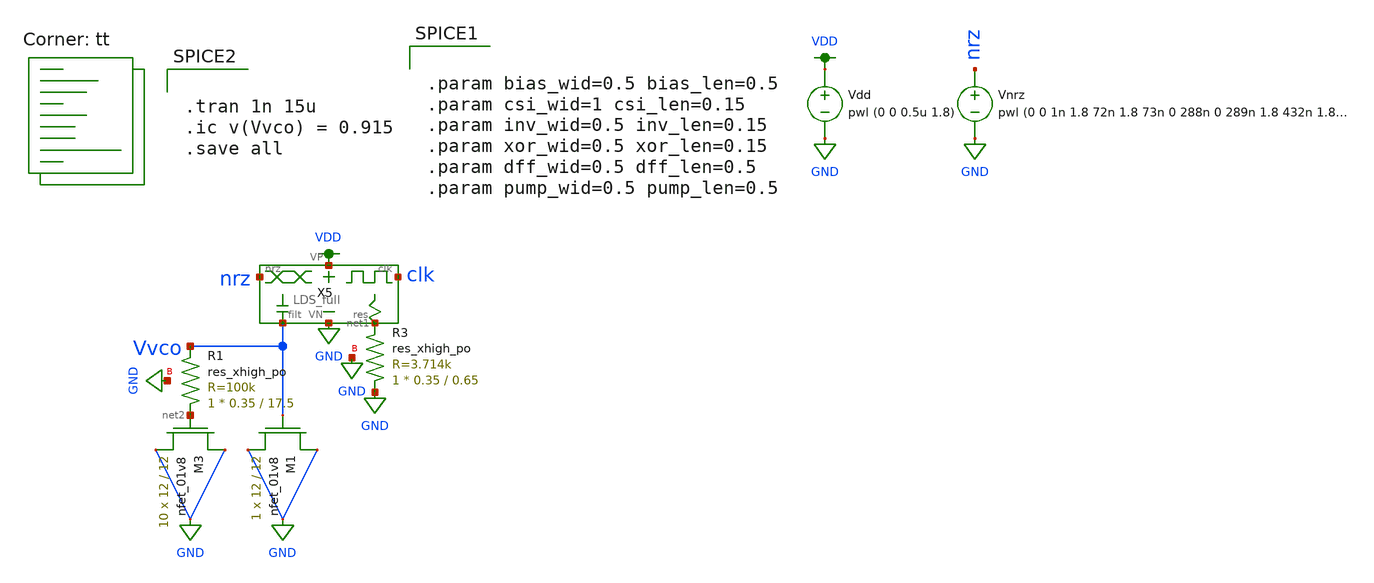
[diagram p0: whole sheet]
** sch_path: LDS/test_full_no_passive.sch
**.subckt test_full_no_passive
Vdd VDD GND pwl (0 0 0.5u 1.8)
Vnrz nrz GND pwl (0 0 1n 1.8 72n 1.8 73n 0 288n 0 289n 1.8 432n 1.8 433n 0 504n 0) R=0 td=1u
X5 VDD GND Vvco nrz net1 clk LDS_full
XM3 GND net2 GND GND sky130_fd_pr__nfet_01v8 L=12 W=12 nf=1 ad='int((nf+1)/2) * W/nf * 0.29' as='int((nf+2)/2) * W/nf * 0.29'
+ pd='2*int((nf+1)/2) * (W/nf + 0.29)' ps='2*int((nf+2)/2) * (W/nf + 0.29)' nrd='0.29 / W' nrs='0.29 / W'
+ sa=0 sb=0 sd=0 mult=10 m=10
XM1 GND Vvco GND GND sky130_fd_pr__nfet_01v8 L=12 W=12 nf=1 ad='int((nf+1)/2) * W/nf * 0.29' as='int((nf+2)/2) * W/nf * 0.29'
+ pd='2*int((nf+1)/2) * (W/nf + 0.29)' ps='2*int((nf+2)/2) * (W/nf + 0.29)' nrd='0.29 / W' nrs='0.29 / W'
+ sa=0 sb=0 sd=0 mult=1 m=1
XR3 GND net1 GND sky130_fd_pr__res_xhigh_po W=0.35 L=0.65 mult=1 m=1
XR1 net2 Vvco GND sky130_fd_pr__res_xhigh_po W=0.35 L=17.5 mult=1 m=1
**** begin user architecture code
.lib $::SKYWATER_MODELS/sky130.lib.spice tt


.tran 1n 15u
.ic v(Vvco) = 0.915
.save all




.param bias_wid=0.5 bias_len=0.5
.param csi_wid=1 csi_len=0.15
.param inv_wid=0.5 inv_len=0.15
.param xor_wid=0.5 xor_len=0.15
.param dff_wid=0.5 dff_len=0.5
.param pump_wid=0.5 pump_len=0.5


**** end user architecture code
**.ends
.GLOBAL VDD
.GLOBAL GND
.end
